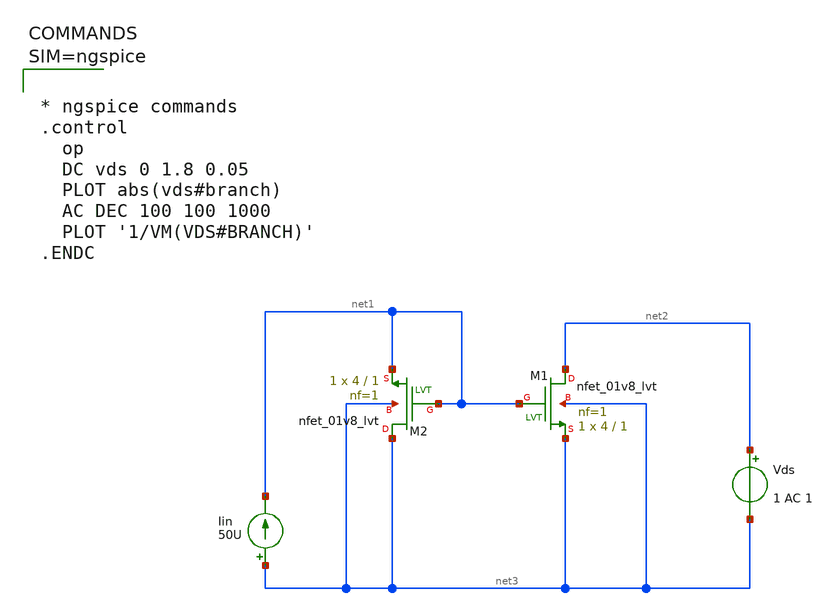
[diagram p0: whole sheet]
** sch_path: xschem/currentmirror.sch
**.subckt currentmirror
XM1 net2 net1 net3 net3 sky130_fd_pr__nfet_01v8_lvt L=1 W=4 nf=1 ad='int((1 + 1)/2) * 4 / 1 * 0.29' as='int((1 + 2)/2) * 4 / 1 * 0.29'
+ pd='2*int((1 + 1)/2) * (4 / 1 + 0.29)' ps='2*int((1 + 2)/2) * (4 / 1 + 0.29)' nrd='0.29 / 4 ' nrs='0.29 / 4 '
+ sa=0 sb=0 sd=0 mult=1 m=1
XM2 net3 net1 net1 net3 sky130_fd_pr__nfet_01v8_lvt L=1 W=4 nf=1 ad='int((1 + 1)/2) * 4 / 1 * 0.29' as='int((1 + 2)/2) * 4 / 1 * 0.29'
+ pd='2*int((1 + 1)/2) * (4 / 1 + 0.29)' ps='2*int((1 + 2)/2) * (4 / 1 + 0.29)' nrd='0.29 / 4 ' nrs='0.29 / 4 '
+ sa=0 sb=0 sd=0 mult=1 m=1
Vds net2 net3 1 AC 1
Iin net3 net1 50U
**** begin user architecture code

** opencircuitdesign pdks install
.lib $::SKYWATER_MODELS/sky130.lib.spice tt




* ngspice commands
.control
  op
  DC vds 0 1.8 0.05
  PLOT abs(vds#branch)
  AC DEC 100 100 1000
  PLOT '1/VM(VDS#BRANCH)'
.ENDC



**** end user architecture code
**.ends
.end
